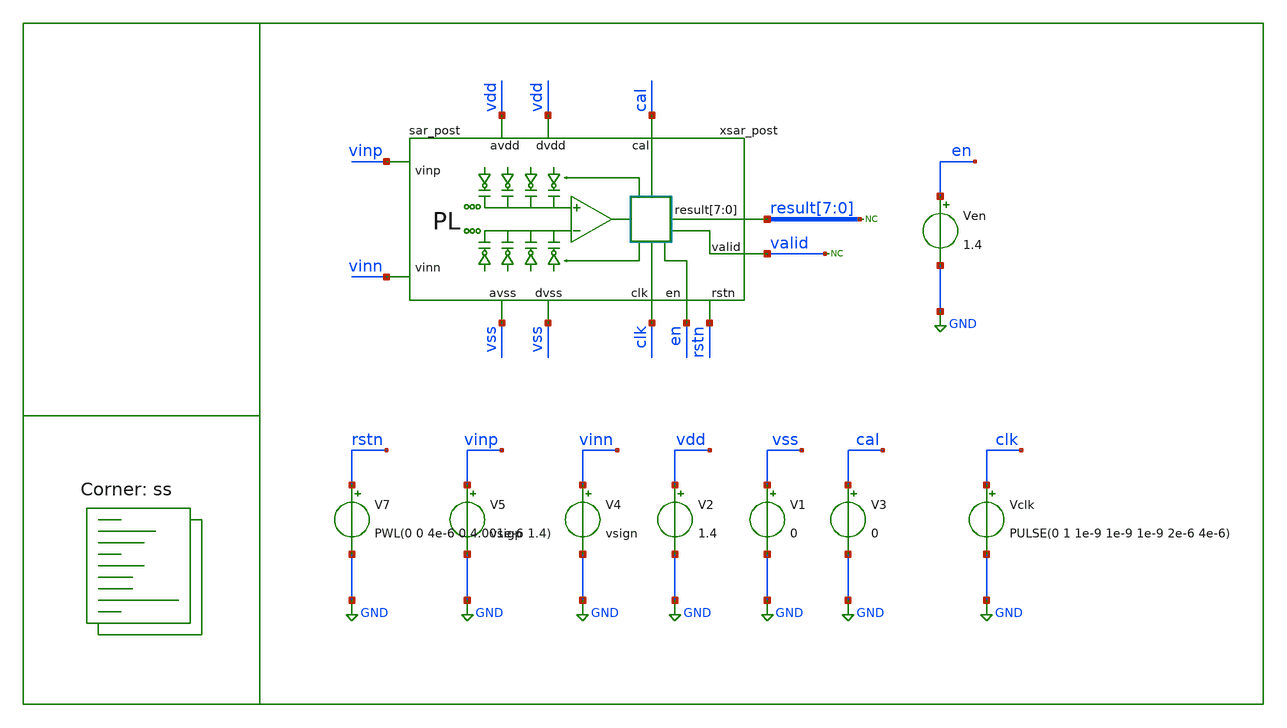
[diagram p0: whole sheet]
** sch_path: full_extract_sim/full_extract_sim.sch

.include /home/alex/Desktop/EDA/SAR_IPN/full_extract_sim/DAC.spice
.include /home/alex/Desktop/EDA/SAR_IPN/full_extract_sim/comparator.spice
.include /home/alex/Desktop/EDA/SAR_IPN/full_extract_sim/latch.spice
.include /home/alex/Desktop/EDA/SAR_IPN/full_extract_sim/sarlogic.spice
*.include /home/alex/Desktop/EDA/SAR_IPN/full_extract_sim/sar/control/cmos_cells_digital.sp
*.include /home/alex/Desktop/EDA/SAR_IPN/full_extract_sim/sar/control/sar_logic.sp
.include $::SKYWATER_STDCELLS/sky130_fd_sc_hd.spice
.include $::SKYWATER_STDCELLS/sky130_ef_sc_hd__decap_12.spice

.lib $::SKYWATER_MODELS/sky130.lib.spice ss
**.subckt full_extract_sim
V1 vss GND 0
V2 vdd GND 1.4
V4 vinn GND vsign
V5 vinp GND vsigp
Vclk clk GND PULSE(0 1 1e-9 1e-9 1e-9 2e-6 4e-6)
Ven en GND 1.4
* noconn valid
V3 cal GND 0
* noconn result[7:0]
xsar_post vdd vdd vss result[7] result[6] result[5] result[4] result[3] result[2] result[1]
+ result[0] vinn vss clk vinp en valid cal rstn sar_post
V7 rstn GND PWL(0 0 4e-6 0 4.001e-6 1.4)
**.ends

* expanding   symbol:  /home/alex/Desktop/EDA/SAR_IPN/full_extract_sim/sar/sar_post/sar_post.sym #
*+ of pins=12
** sym_path: full_extract_sim/sar/sar_post/sar_post.sym
** sch_path: full_extract_sim/sar/sar_post/sar_post.sch
.subckt sar_post avdd dvdd dvss result[7] result[6] result[5] result[4] result[3] result[2]
+ result[1] result[0] vinn avss clk vinp en valid cal rstn
*.iopin avss
*.iopin avdd
*.iopin dvss
*.iopin dvdd
*.ipin vinp
*.ipin vinn
*.opin result[7],result[6],result[5],result[4],result[3],result[2],result[1],result[0]
*.ipin clk
*.ipin en
*.opin valid
*.ipin cal
*.ipin rstn
xlat avdd avss net1 outp outn comp latch
* noconn #net1
* noconn comp
* noconn sample
* noconn ctln[7:0]
* noconn ctlp[7:0]
* noconn trim[4:0]
* noconn trimb[4:0]
* noconn result[7:0]
* noconn valid
* noconn clkc
* noconn clk
* noconn en
* noconn cal
xdn n_sample sample ctln[1] ctln[0] avss ctln[3] ctln[4] ctln[5] ctln[6] ctln[7] ctln[2] avdd avss
+ sample vn vinn DAC
xcom trim[3] trim[2] trim[0] trim[1] trim[4] trimb[4] trimb[1] trimb[0] trimb[2] trimb[3] outn outp
+ clkc avdd avss vn vp comparator
* noconn rstn
**** begin user architecture code


.model adc_buff adc_bridge(in_low = 0.2 in_high=0.8)
.model dac_buff dac_bridge(out_high = 1.2)

Aad [clk rstn en comp cal] [dclk drstn den dcomp dcal] adc_buff
Ada [dctlp0 dctlp1 dctlp2 dctlp3 dctlp4 dctlp5 dctlp6 dctlp7 dctln0 dctln1 dctln2 dctln3 dctln4
+ dctln5 dctln6 dctln7 dres0 dres1 dres2 dres3 dres4 dres5 dres6 dres7 dsamp dclkc] [ctlp_0_ ctlp_1_ ctlp_2_
+ ctlp_3_ ctlp_4_ ctlp_5_ ctlp_6_ ctlp_7_ ctln_0_ ctln_1_ ctln_2_ ctln_3_ ctln_4_ ctln_5_ ctln_6_ ctln_7_
+ res0 res1 res2 res3 res4 res5 res6 res7 sample clkc] dac_buff
Ada2 [dtrim4 dtrim3 dtrim2 dtrim1 dtrim0 dtrimb4 dtrimb3 dtrimb2 dtrimb1 dtrimb0] [trim_4_ trim_3_
+ trim_2_ trim_1_ trim_0_ trimb_4_ trimb_3_ trimb_2_ trimb_1_ trimb_0_ ] dac_buff

Xuut dvss dvdd dcal dclk dclkc dcomp dctln0 dctln1 dctln2 dctln3 dctln4 dctln5 dctln6 dctln7 dctlp0
+ dctlp1 dctlp2 dctlp3 dctlp4 dctlp5 dctlp6 dctlp7  den dres0 dres1 dres2 dres3 dres4 dres5 dres6 dres7
+ drstn dsamp dtrim0 dtrim1 dtrim2 dtrim3 dtrim4 dtrimb0 dtrimb1 dtrimb2 dtrimb3 dtrimb4 dvalid sar_logic



**** end user architecture code
xdp n_sample sample ctlp[1] ctlp[0] avdd ctlp[3] ctlp[4] ctlp[5] ctlp[6] ctlp[7] ctlp[2] avdd avss
+ sample vp vinp DAC
x1 sample VGND VNB VPB VPWR n_sample sky130_fd_sc_hd__inv_1
.ends

.GLOBAL GND
**** begin user architecture code

.options method trap
*.options method gear
.options gmin 1e-15
.options abstol 1e-15
.options reltol 0.0001
.options vntol 0.1e-6
.options warn 1

.param MC_SWITCH=0
.param vin=0.1
.param vcm=0.7
.param vsigp={vcm + vin/2}
.param vsign={vcm - vin/2}

.tran 100e-9 48e-6
.save all
.control

run
write full_extract_sim_digital.raw
meas tran d0 find v(xsar_post.res0) at=47e-6
meas tran d1 find v(xsar_post.res1) at=47e-6
meas tran d2 find v(xsar_post.res2) at=47e-6
meas tran d3 find v(xsar_post.res3) at=47e-6
meas tran d4 find v(xsar_post.res4) at=47e-6
meas tran d5 find v(xsar_post.res5) at=47e-6
meas tran d6 find v(xsar_post.res6) at=47e-6
meas tran d7 find v(xsar_post.res7) at=47e-6

* meas tran d0 find v(xsar.result0) at=47e-6
* meas tran d1 find v(xsar.result1) at=47e-6
* meas tran d2 find v(xsar.result2) at=47e-6
* meas tran d3 find v(xsar.result3) at=47e-6
* meas tran d4 find v(xsar.result4) at=47e-6
* meas tran d5 find v(xsar.result5) at=47e-6
* meas tran d6 find v(xsar.result6) at=47e-6
* meas tran d7 find v(xsar.result7) at=47e-6

meas tran vpmax max xsar_post.vp
meas tran vpmin min xsar_post.vp
meas tran vpend find v(xsar_post.vp) at=39e-6

meas tran vnmax max xsar_post.vn
meas tran vnmin min xsar_post.vn
meas tran vnend find v(xsar_post.vn) at=39e-6

print d0
print d1
print d2
print d3
print d4
print d5
print d6
print d7

print vpmax
print vpmin

print vnmax
print vnmin

print vpend
print vnend

.endc


**** end user architecture code
.end
